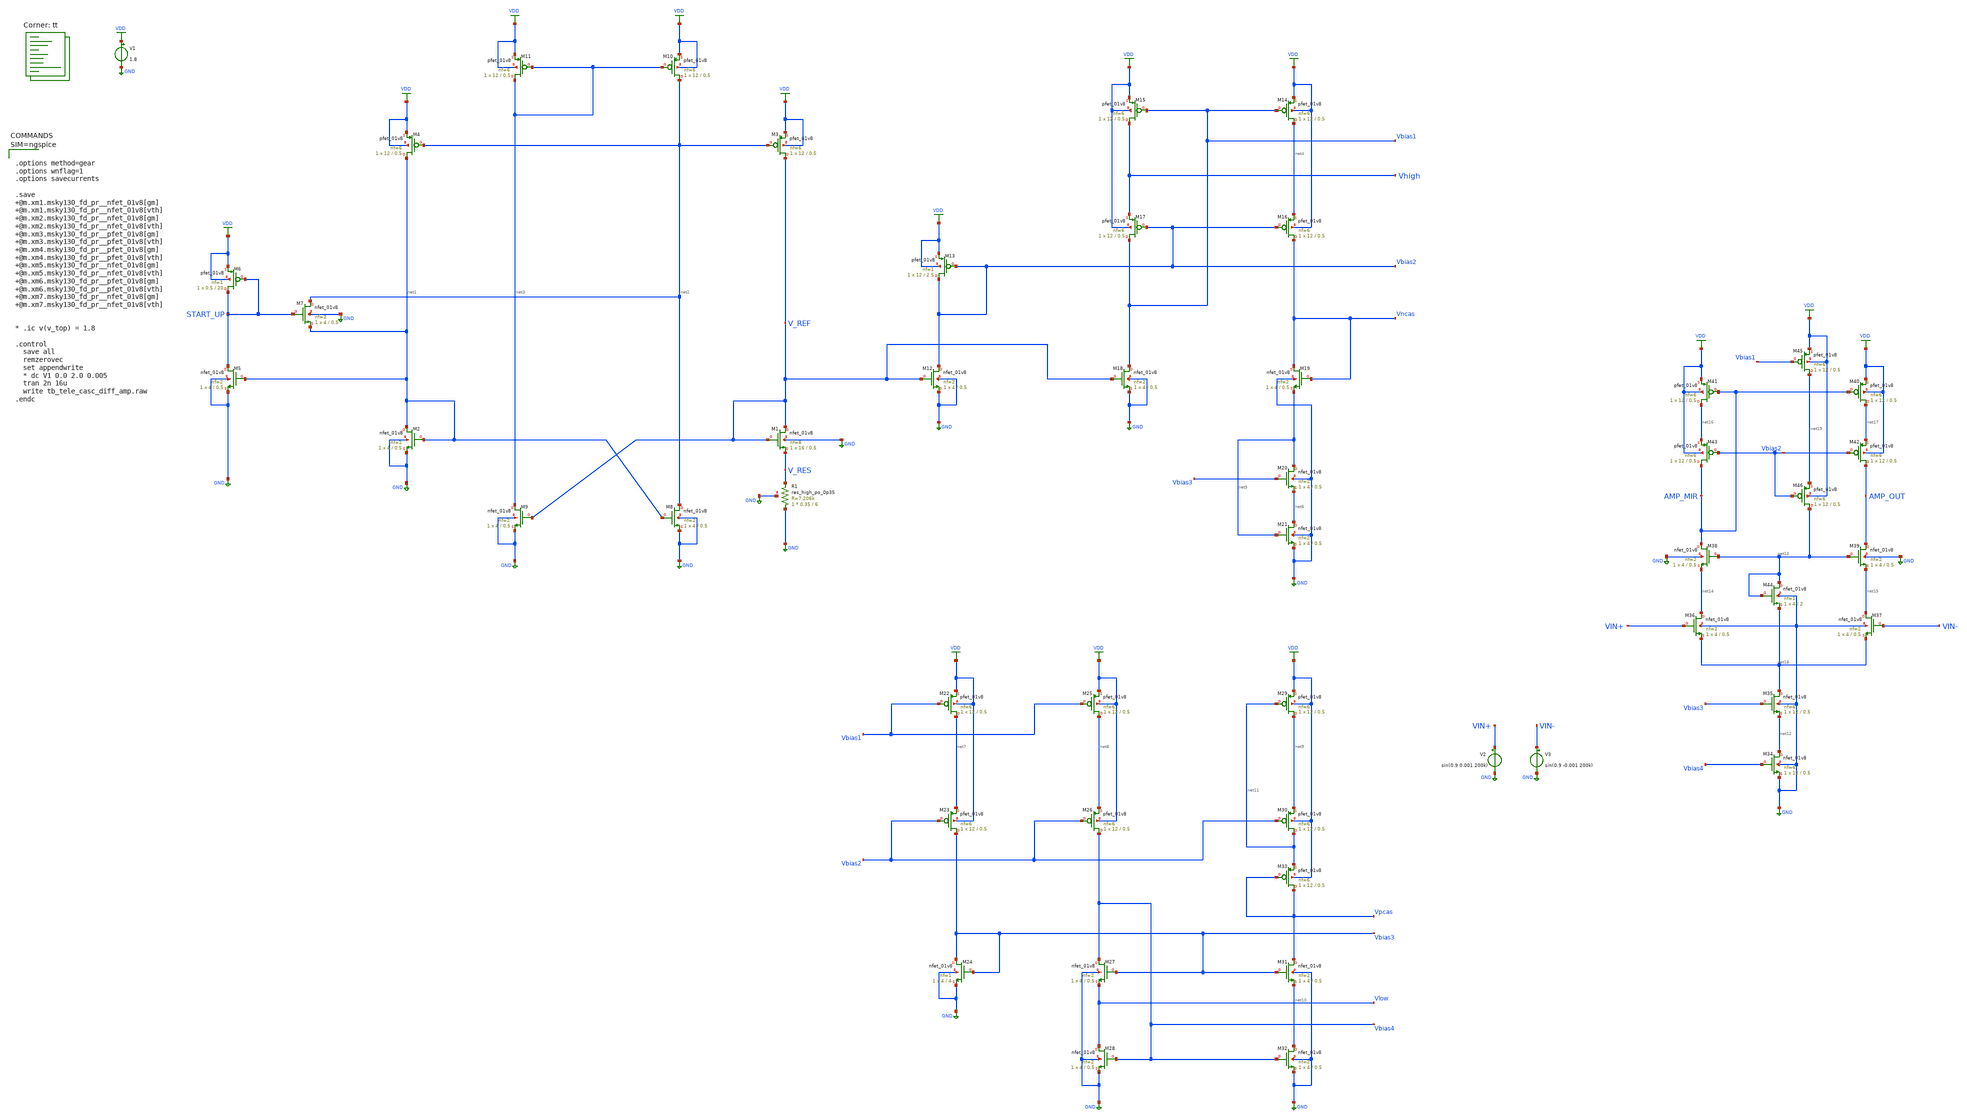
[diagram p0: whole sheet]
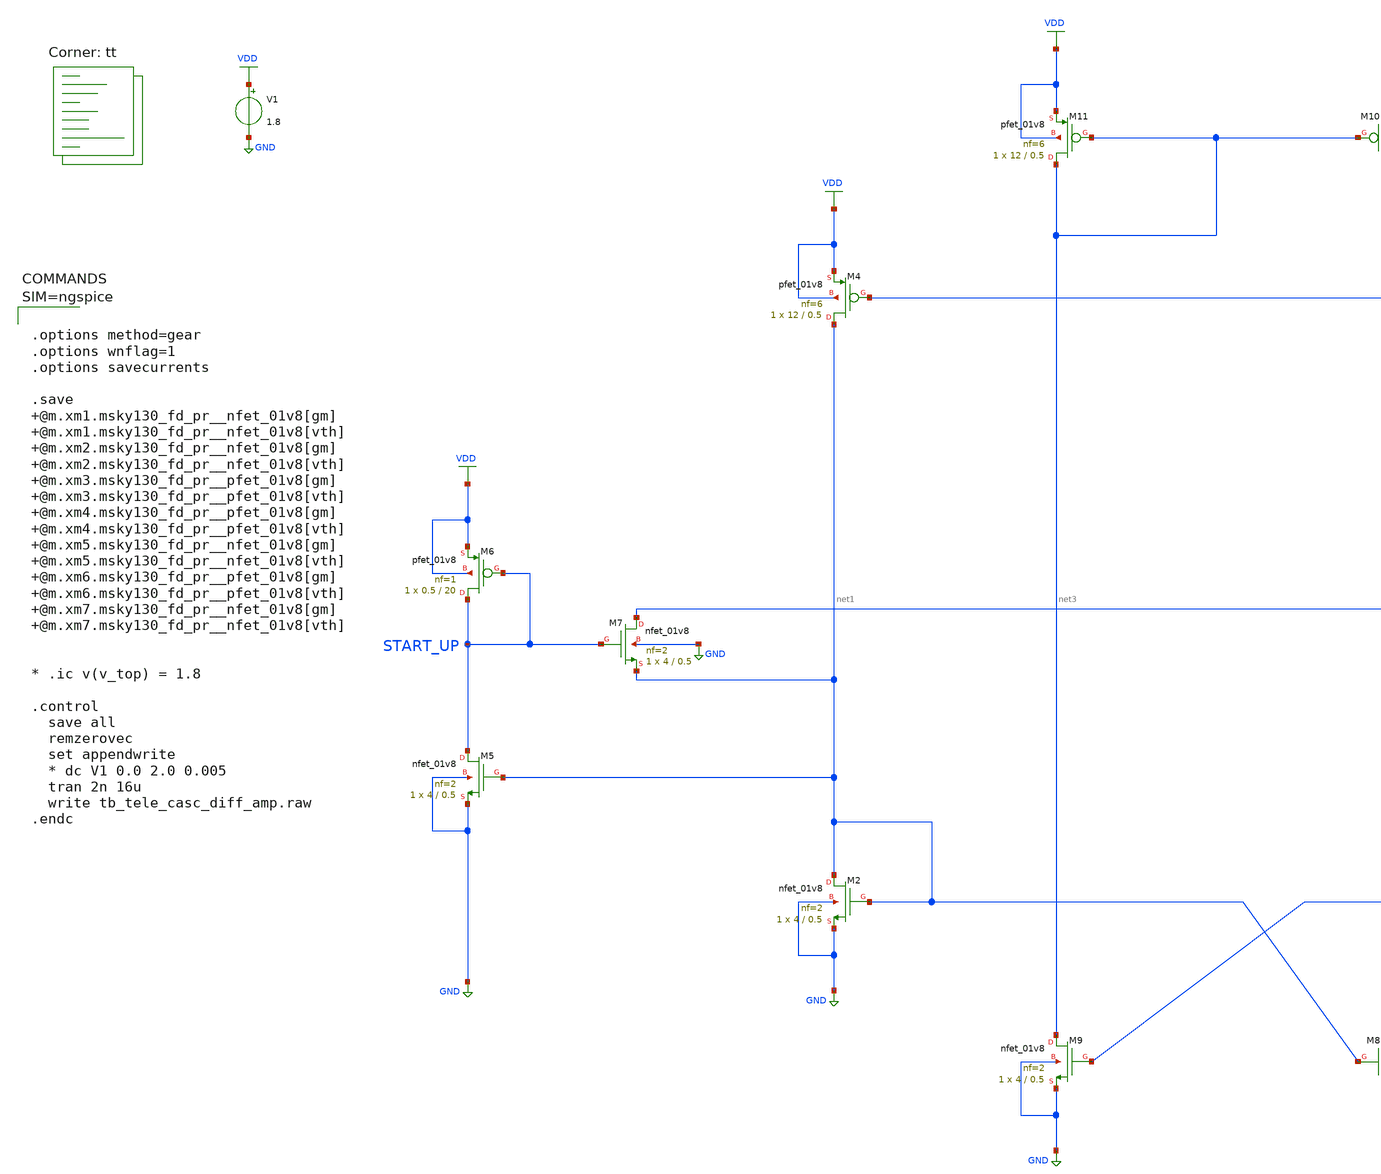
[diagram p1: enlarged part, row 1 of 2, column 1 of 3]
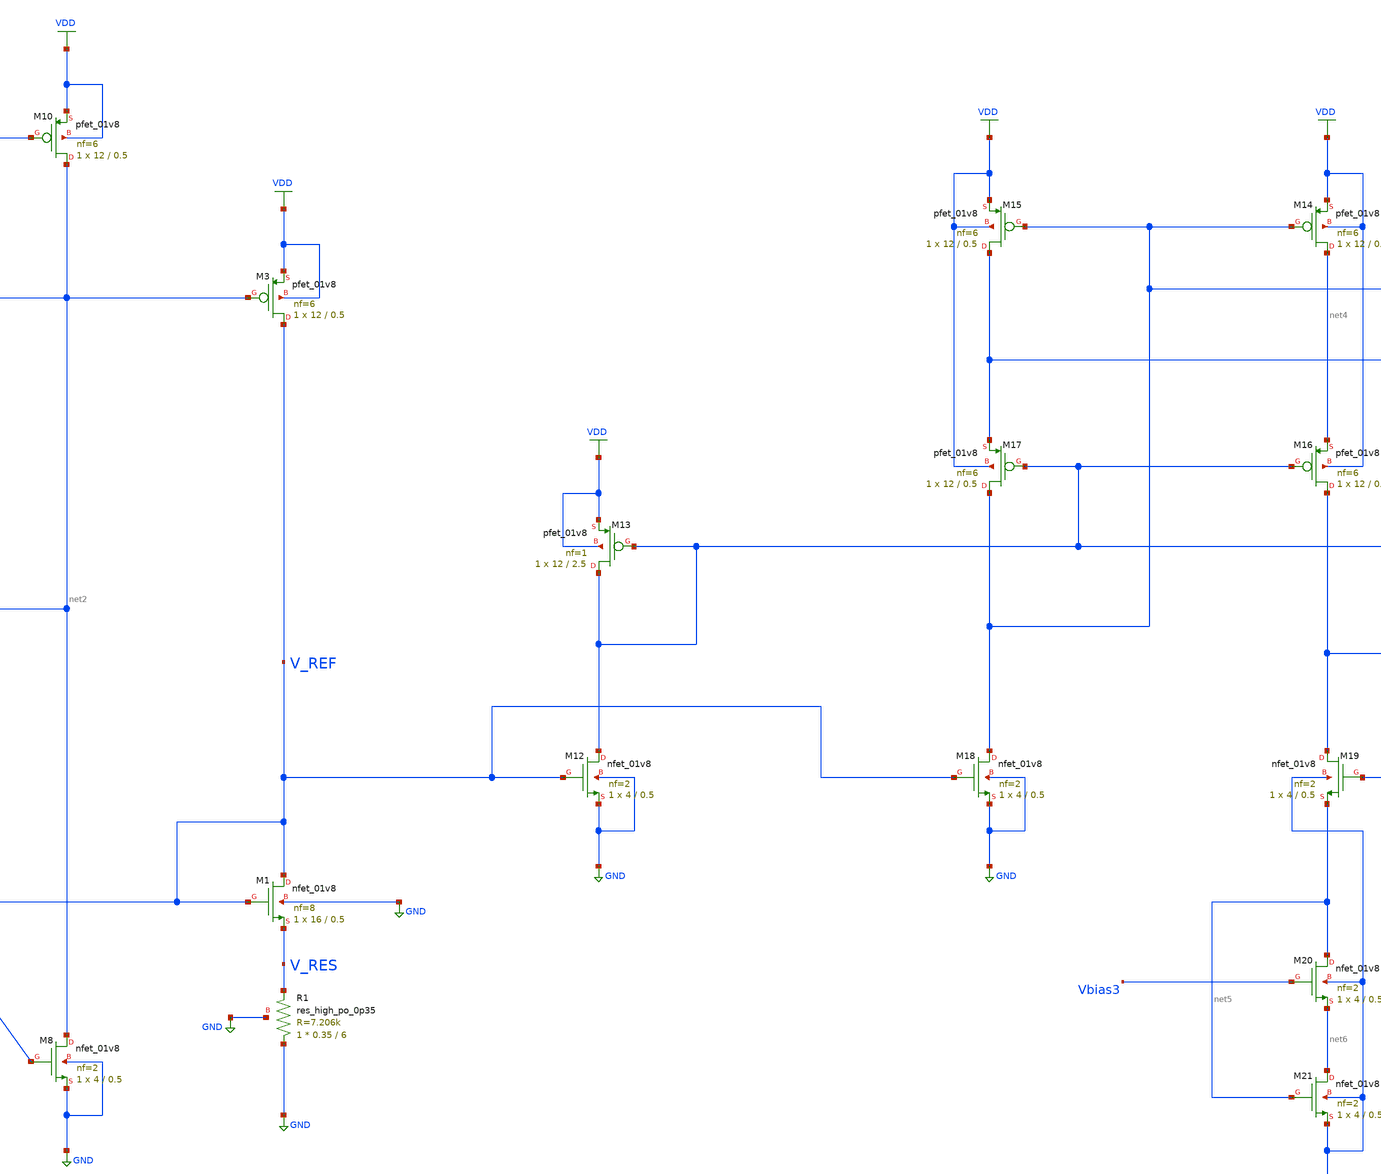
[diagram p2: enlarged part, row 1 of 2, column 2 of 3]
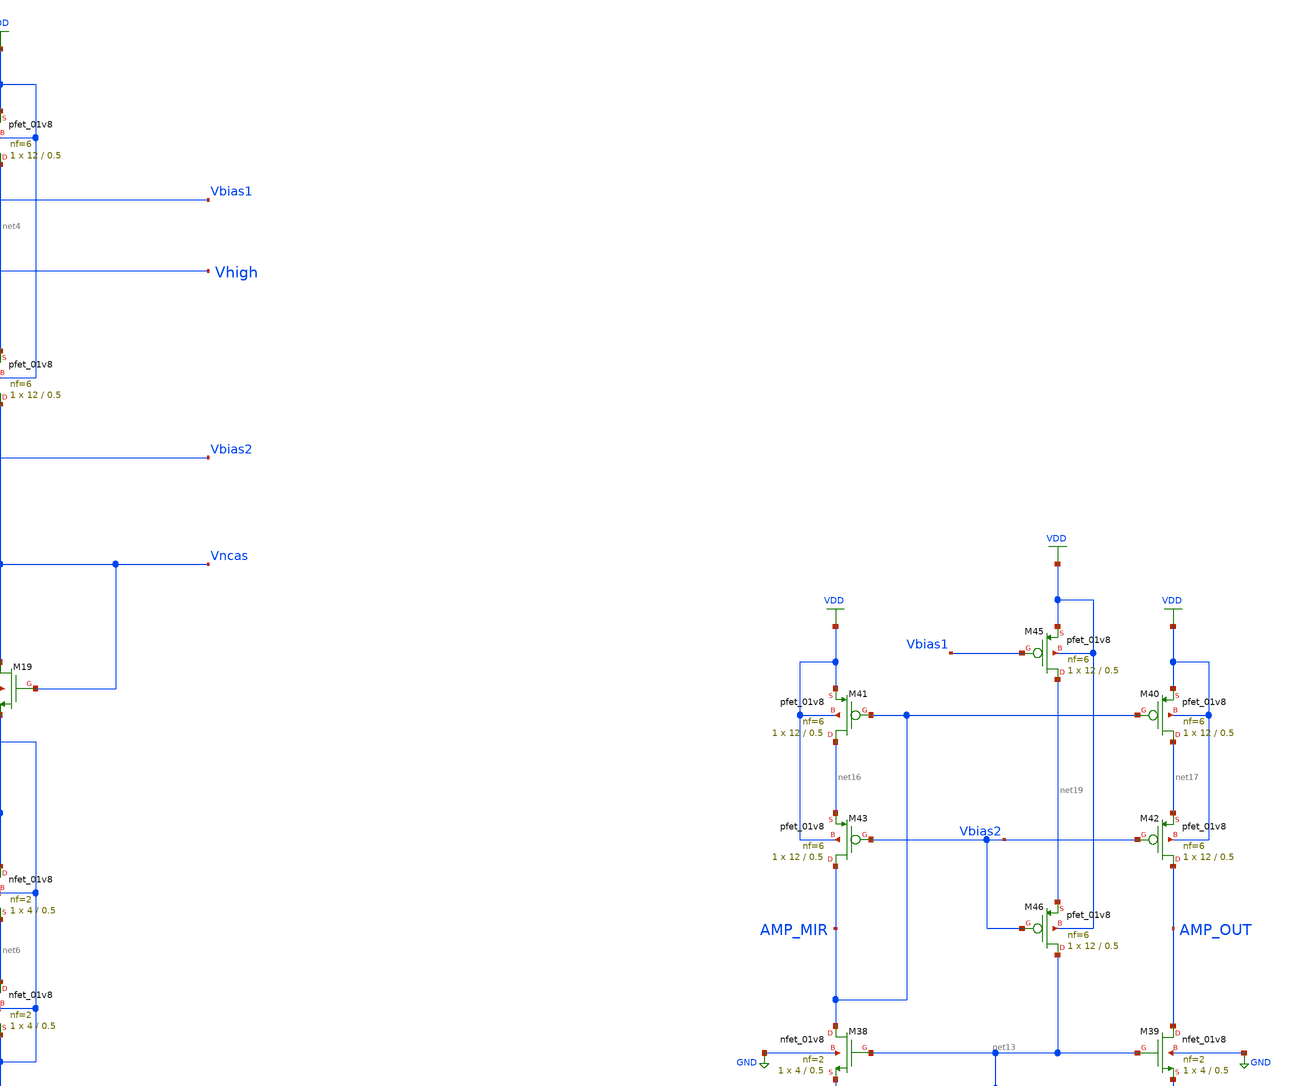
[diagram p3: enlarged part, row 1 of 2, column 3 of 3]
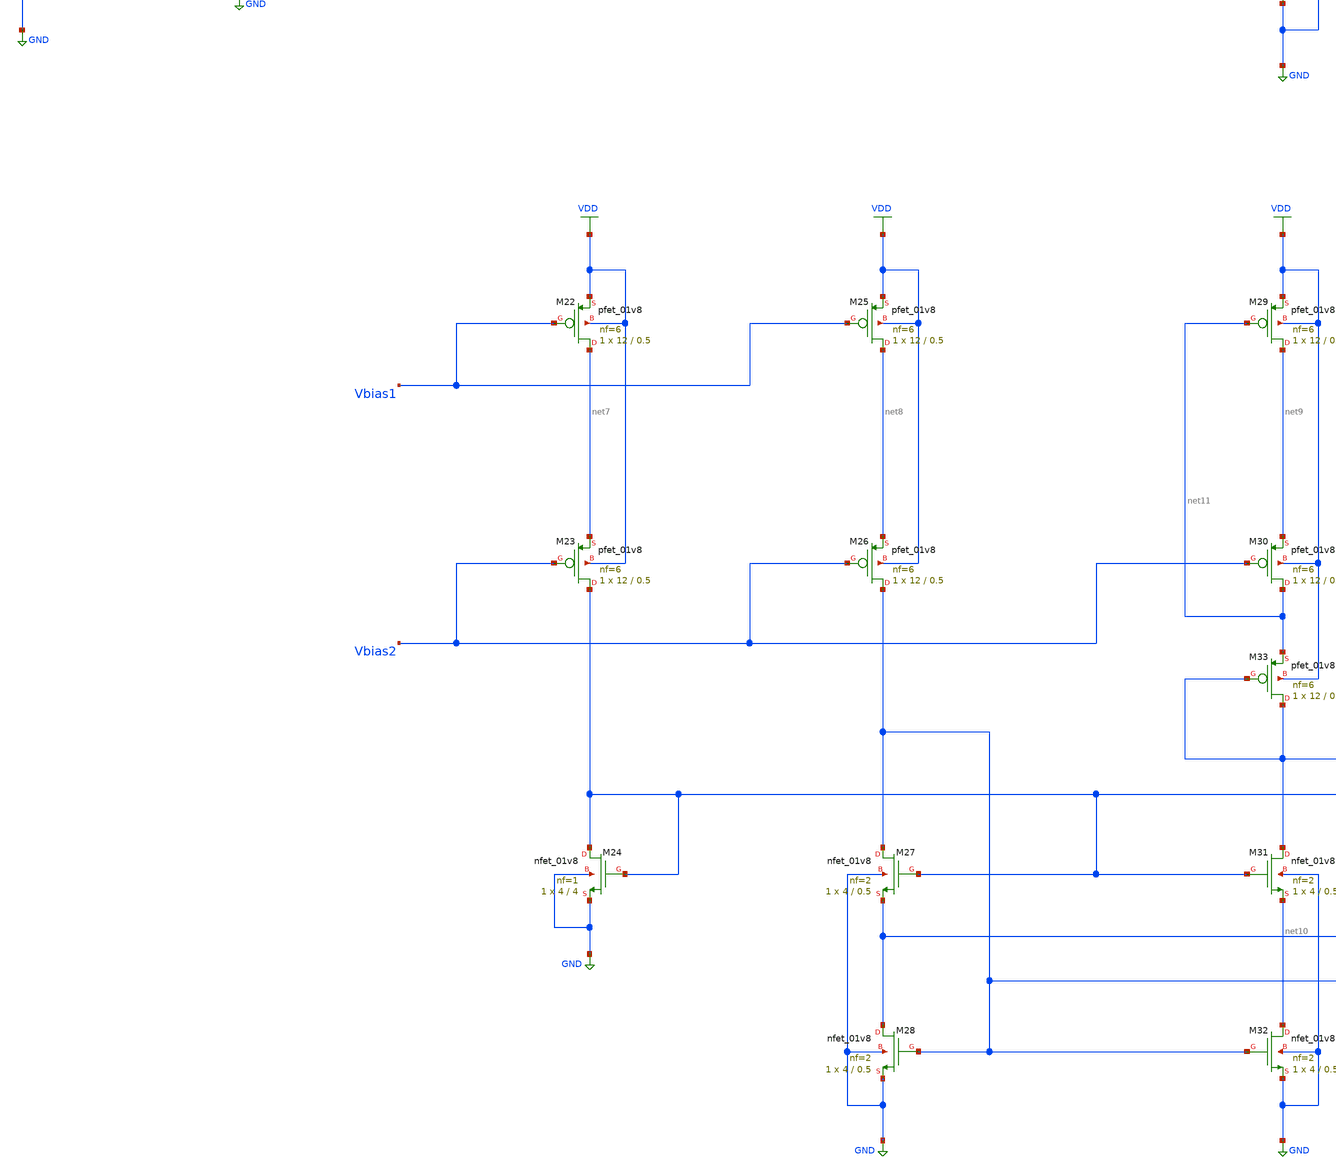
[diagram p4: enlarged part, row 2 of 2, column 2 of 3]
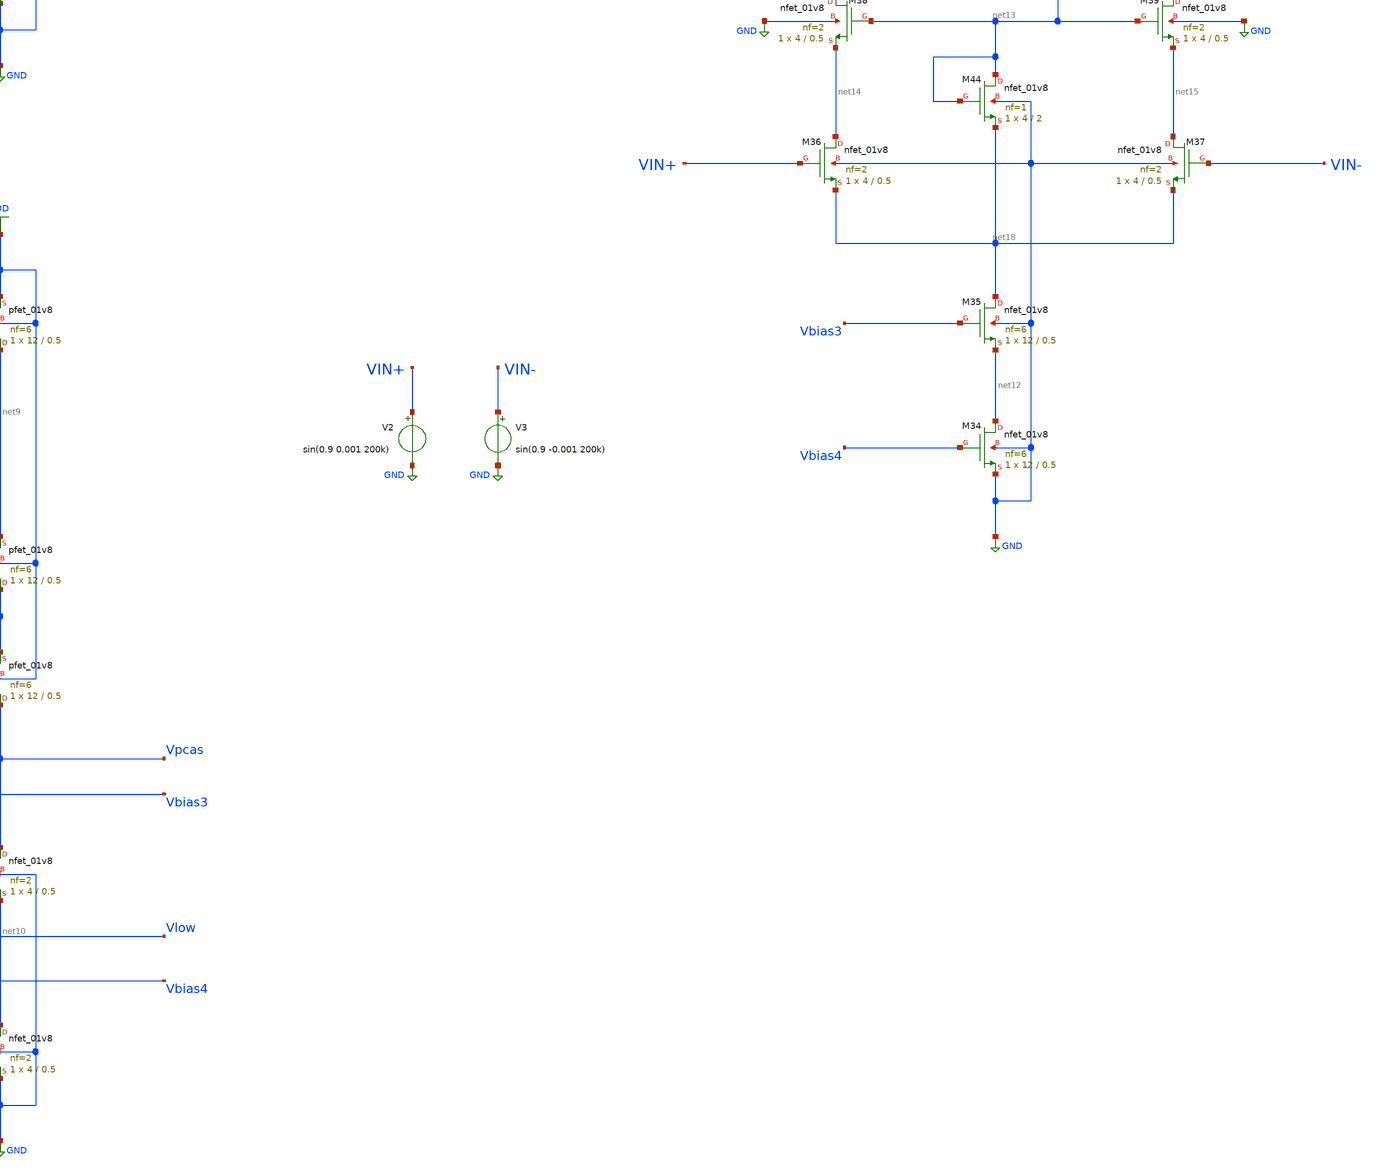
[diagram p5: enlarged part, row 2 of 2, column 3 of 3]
** sch_path: projects/ASU/EEE572/schematic/tb_tele_casc_diff_amp.sch
**.subckt tb_tele_casc_diff_amp
V1 VDD GND 1.8
XM1 V_REF V_REF V_RES GND sky130_fd_pr__nfet_01v8 L=0.5 W=16 nf=8 ad='int((nf+1)/2) * W/nf * 0.29' as='int((nf+2)/2) * W/nf * 0.29'
+ pd='2*int((nf+1)/2) * (W/nf + 0.29)' ps='2*int((nf+2)/2) * (W/nf + 0.29)' nrd='0.29 / W' nrs='0.29 / W'
+ sa=0 sb=0 sd=0 mult=1 m=1
XM2 net1 net1 GND GND sky130_fd_pr__nfet_01v8 L=0.5 W=4 nf=2 ad='int((nf+1)/2) * W/nf * 0.29' as='int((nf+2)/2) * W/nf * 0.29'
+ pd='2*int((nf+1)/2) * (W/nf + 0.29)' ps='2*int((nf+2)/2) * (W/nf + 0.29)' nrd='0.29 / W' nrs='0.29 / W'
+ sa=0 sb=0 sd=0 mult=1 m=1
XM5 START_UP net1 GND GND sky130_fd_pr__nfet_01v8 L=0.5 W=4 nf=2 ad='int((nf+1)/2) * W/nf * 0.29' as='int((nf+2)/2) * W/nf * 0.29'
+ pd='2*int((nf+1)/2) * (W/nf + 0.29)' ps='2*int((nf+2)/2) * (W/nf + 0.29)' nrd='0.29 / W' nrs='0.29 / W'
+ sa=0 sb=0 sd=0 mult=1 m=1
XM7 net2 START_UP net1 GND sky130_fd_pr__nfet_01v8 L=0.5 W=4 nf=2 ad='int((nf+1)/2) * W/nf * 0.29' as='int((nf+2)/2) * W/nf * 0.29'
+ pd='2*int((nf+1)/2) * (W/nf + 0.29)' ps='2*int((nf+2)/2) * (W/nf + 0.29)' nrd='0.29 / W' nrs='0.29 / W'
+ sa=0 sb=0 sd=0 mult=1 m=1
XR1 GND V_RES GND sky130_fd_pr__res_high_po_0p35 L=6 mult=1 m=1
XM6 START_UP START_UP VDD VDD sky130_fd_pr__pfet_01v8 L=20 W=0.5 nf=1 ad='int((nf+1)/2) * W/nf * 0.29'
+ as='int((nf+2)/2) * W/nf * 0.29' pd='2*int((nf+1)/2) * (W/nf + 0.29)' ps='2*int((nf+2)/2) * (W/nf + 0.29)'
+ nrd='0.29 / W' nrs='0.29 / W' sa=0 sb=0 sd=0 mult=1 m=1
XM3 V_REF net2 VDD VDD sky130_fd_pr__pfet_01v8 L=0.5 W=12 nf=6 ad='int((nf+1)/2) * W/nf * 0.29' as='int((nf+2)/2) * W/nf * 0.29'
+ pd='2*int((nf+1)/2) * (W/nf + 0.29)' ps='2*int((nf+2)/2) * (W/nf + 0.29)' nrd='0.29 / W' nrs='0.29 / W'
+ sa=0 sb=0 sd=0 mult=1 m=1
XM4 net1 net2 VDD VDD sky130_fd_pr__pfet_01v8 L=0.5 W=12 nf=6 ad='int((nf+1)/2) * W/nf * 0.29' as='int((nf+2)/2) * W/nf * 0.29'
+ pd='2*int((nf+1)/2) * (W/nf + 0.29)' ps='2*int((nf+2)/2) * (W/nf + 0.29)' nrd='0.29 / W' nrs='0.29 / W'
+ sa=0 sb=0 sd=0 mult=1 m=1
XM8 net2 net1 GND GND sky130_fd_pr__nfet_01v8 L=0.5 W=4 nf=2 ad='int((nf+1)/2) * W/nf * 0.29' as='int((nf+2)/2) * W/nf * 0.29'
+ pd='2*int((nf+1)/2) * (W/nf + 0.29)' ps='2*int((nf+2)/2) * (W/nf + 0.29)' nrd='0.29 / W' nrs='0.29 / W'
+ sa=0 sb=0 sd=0 mult=1 m=1
XM9 net3 V_REF GND GND sky130_fd_pr__nfet_01v8 L=0.5 W=4 nf=2 ad='int((nf+1)/2) * W/nf * 0.29' as='int((nf+2)/2) * W/nf * 0.29'
+ pd='2*int((nf+1)/2) * (W/nf + 0.29)' ps='2*int((nf+2)/2) * (W/nf + 0.29)' nrd='0.29 / W' nrs='0.29 / W'
+ sa=0 sb=0 sd=0 mult=1 m=1
XM10 net2 net3 VDD VDD sky130_fd_pr__pfet_01v8 L=0.5 W=12 nf=6 ad='int((nf+1)/2) * W/nf * 0.29' as='int((nf+2)/2) * W/nf * 0.29'
+ pd='2*int((nf+1)/2) * (W/nf + 0.29)' ps='2*int((nf+2)/2) * (W/nf + 0.29)' nrd='0.29 / W' nrs='0.29 / W'
+ sa=0 sb=0 sd=0 mult=1 m=1
XM11 net3 net3 VDD VDD sky130_fd_pr__pfet_01v8 L=0.5 W=12 nf=6 ad='int((nf+1)/2) * W/nf * 0.29' as='int((nf+2)/2) * W/nf * 0.29'
+ pd='2*int((nf+1)/2) * (W/nf + 0.29)' ps='2*int((nf+2)/2) * (W/nf + 0.29)' nrd='0.29 / W' nrs='0.29 / W'
+ sa=0 sb=0 sd=0 mult=1 m=1
XM12 Vbias2 V_REF GND GND sky130_fd_pr__nfet_01v8 L=0.5 W=4 nf=2 ad='int((nf+1)/2) * W/nf * 0.29' as='int((nf+2)/2) * W/nf * 0.29'
+ pd='2*int((nf+1)/2) * (W/nf + 0.29)' ps='2*int((nf+2)/2) * (W/nf + 0.29)' nrd='0.29 / W' nrs='0.29 / W'
+ sa=0 sb=0 sd=0 mult=1 m=1
XM13 Vbias2 Vbias2 VDD VDD sky130_fd_pr__pfet_01v8 L=2.5 W=12 nf=1 ad='int((nf+1)/2) * W/nf * 0.29' as='int((nf+2)/2) * W/nf * 0.29'
+ pd='2*int((nf+1)/2) * (W/nf + 0.29)' ps='2*int((nf+2)/2) * (W/nf + 0.29)' nrd='0.29 / W' nrs='0.29 / W'
+ sa=0 sb=0 sd=0 mult=1 m=1
XM14 net4 Vbias1 VDD VDD sky130_fd_pr__pfet_01v8 L=0.5 W=12 nf=6 ad='int((nf+1)/2) * W/nf * 0.29' as='int((nf+2)/2) * W/nf * 0.29'
+ pd='2*int((nf+1)/2) * (W/nf + 0.29)' ps='2*int((nf+2)/2) * (W/nf + 0.29)' nrd='0.29 / W' nrs='0.29 / W'
+ sa=0 sb=0 sd=0 mult=1 m=1
XM15 Vhigh Vbias1 VDD VDD sky130_fd_pr__pfet_01v8 L=0.5 W=12 nf=6 ad='int((nf+1)/2) * W/nf * 0.29' as='int((nf+2)/2) * W/nf * 0.29'
+ pd='2*int((nf+1)/2) * (W/nf + 0.29)' ps='2*int((nf+2)/2) * (W/nf + 0.29)' nrd='0.29 / W' nrs='0.29 / W'
+ sa=0 sb=0 sd=0 mult=1 m=1
XM16 Vncas Vbias2 net4 VDD sky130_fd_pr__pfet_01v8 L=0.5 W=12 nf=6 ad='int((nf+1)/2) * W/nf * 0.29' as='int((nf+2)/2) * W/nf * 0.29'
+ pd='2*int((nf+1)/2) * (W/nf + 0.29)' ps='2*int((nf+2)/2) * (W/nf + 0.29)' nrd='0.29 / W' nrs='0.29 / W'
+ sa=0 sb=0 sd=0 mult=1 m=1
XM17 Vbias1 Vbias2 Vhigh VDD sky130_fd_pr__pfet_01v8 L=0.5 W=12 nf=6 ad='int((nf+1)/2) * W/nf * 0.29'
+ as='int((nf+2)/2) * W/nf * 0.29' pd='2*int((nf+1)/2) * (W/nf + 0.29)' ps='2*int((nf+2)/2) * (W/nf + 0.29)'
+ nrd='0.29 / W' nrs='0.29 / W' sa=0 sb=0 sd=0 mult=1 m=1
XM18 Vbias1 V_REF GND GND sky130_fd_pr__nfet_01v8 L=0.5 W=4 nf=2 ad='int((nf+1)/2) * W/nf * 0.29' as='int((nf+2)/2) * W/nf * 0.29'
+ pd='2*int((nf+1)/2) * (W/nf + 0.29)' ps='2*int((nf+2)/2) * (W/nf + 0.29)' nrd='0.29 / W' nrs='0.29 / W'
+ sa=0 sb=0 sd=0 mult=1 m=1
XM19 Vncas Vncas net5 GND sky130_fd_pr__nfet_01v8 L=0.5 W=4 nf=2 ad='int((nf+1)/2) * W/nf * 0.29' as='int((nf+2)/2) * W/nf * 0.29'
+ pd='2*int((nf+1)/2) * (W/nf + 0.29)' ps='2*int((nf+2)/2) * (W/nf + 0.29)' nrd='0.29 / W' nrs='0.29 / W'
+ sa=0 sb=0 sd=0 mult=1 m=1
XM20 net5 Vbias3 net6 GND sky130_fd_pr__nfet_01v8 L=0.5 W=4 nf=2 ad='int((nf+1)/2) * W/nf * 0.29' as='int((nf+2)/2) * W/nf * 0.29'
+ pd='2*int((nf+1)/2) * (W/nf + 0.29)' ps='2*int((nf+2)/2) * (W/nf + 0.29)' nrd='0.29 / W' nrs='0.29 / W'
+ sa=0 sb=0 sd=0 mult=1 m=1
XM21 net6 net5 GND GND sky130_fd_pr__nfet_01v8 L=0.5 W=4 nf=2 ad='int((nf+1)/2) * W/nf * 0.29' as='int((nf+2)/2) * W/nf * 0.29'
+ pd='2*int((nf+1)/2) * (W/nf + 0.29)' ps='2*int((nf+2)/2) * (W/nf + 0.29)' nrd='0.29 / W' nrs='0.29 / W'
+ sa=0 sb=0 sd=0 mult=1 m=1
XM22 net7 Vbias1 VDD VDD sky130_fd_pr__pfet_01v8 L=0.5 W=12 nf=6 ad='int((nf+1)/2) * W/nf * 0.29' as='int((nf+2)/2) * W/nf * 0.29'
+ pd='2*int((nf+1)/2) * (W/nf + 0.29)' ps='2*int((nf+2)/2) * (W/nf + 0.29)' nrd='0.29 / W' nrs='0.29 / W'
+ sa=0 sb=0 sd=0 mult=1 m=1
XM23 Vbias3 Vbias2 net7 VDD sky130_fd_pr__pfet_01v8 L=0.5 W=12 nf=6 ad='int((nf+1)/2) * W/nf * 0.29'
+ as='int((nf+2)/2) * W/nf * 0.29' pd='2*int((nf+1)/2) * (W/nf + 0.29)' ps='2*int((nf+2)/2) * (W/nf + 0.29)'
+ nrd='0.29 / W' nrs='0.29 / W' sa=0 sb=0 sd=0 mult=1 m=1
XM24 Vbias3 Vbias3 GND GND sky130_fd_pr__nfet_01v8 L=4 W=4 nf=1 ad='int((nf+1)/2) * W/nf * 0.29' as='int((nf+2)/2) * W/nf * 0.29'
+ pd='2*int((nf+1)/2) * (W/nf + 0.29)' ps='2*int((nf+2)/2) * (W/nf + 0.29)' nrd='0.29 / W' nrs='0.29 / W'
+ sa=0 sb=0 sd=0 mult=1 m=1
XM25 net8 Vbias1 VDD VDD sky130_fd_pr__pfet_01v8 L=0.5 W=12 nf=6 ad='int((nf+1)/2) * W/nf * 0.29' as='int((nf+2)/2) * W/nf * 0.29'
+ pd='2*int((nf+1)/2) * (W/nf + 0.29)' ps='2*int((nf+2)/2) * (W/nf + 0.29)' nrd='0.29 / W' nrs='0.29 / W'
+ sa=0 sb=0 sd=0 mult=1 m=1
XM26 Vbias4 Vbias2 net8 VDD sky130_fd_pr__pfet_01v8 L=0.5 W=12 nf=6 ad='int((nf+1)/2) * W/nf * 0.29'
+ as='int((nf+2)/2) * W/nf * 0.29' pd='2*int((nf+1)/2) * (W/nf + 0.29)' ps='2*int((nf+2)/2) * (W/nf + 0.29)'
+ nrd='0.29 / W' nrs='0.29 / W' sa=0 sb=0 sd=0 mult=1 m=1
XM27 Vbias4 Vbias3 Vlow GND sky130_fd_pr__nfet_01v8 L=0.5 W=4 nf=2 ad='int((nf+1)/2) * W/nf * 0.29' as='int((nf+2)/2) * W/nf * 0.29'
+ pd='2*int((nf+1)/2) * (W/nf + 0.29)' ps='2*int((nf+2)/2) * (W/nf + 0.29)' nrd='0.29 / W' nrs='0.29 / W'
+ sa=0 sb=0 sd=0 mult=1 m=1
XM28 Vlow Vbias4 GND GND sky130_fd_pr__nfet_01v8 L=0.5 W=4 nf=2 ad='int((nf+1)/2) * W/nf * 0.29' as='int((nf+2)/2) * W/nf * 0.29'
+ pd='2*int((nf+1)/2) * (W/nf + 0.29)' ps='2*int((nf+2)/2) * (W/nf + 0.29)' nrd='0.29 / W' nrs='0.29 / W'
+ sa=0 sb=0 sd=0 mult=1 m=1
XM29 net9 net11 VDD VDD sky130_fd_pr__pfet_01v8 L=0.5 W=12 nf=6 ad='int((nf+1)/2) * W/nf * 0.29' as='int((nf+2)/2) * W/nf * 0.29'
+ pd='2*int((nf+1)/2) * (W/nf + 0.29)' ps='2*int((nf+2)/2) * (W/nf + 0.29)' nrd='0.29 / W' nrs='0.29 / W'
+ sa=0 sb=0 sd=0 mult=1 m=1
XM30 net11 Vbias2 net9 VDD sky130_fd_pr__pfet_01v8 L=0.5 W=12 nf=6 ad='int((nf+1)/2) * W/nf * 0.29' as='int((nf+2)/2) * W/nf * 0.29'
+ pd='2*int((nf+1)/2) * (W/nf + 0.29)' ps='2*int((nf+2)/2) * (W/nf + 0.29)' nrd='0.29 / W' nrs='0.29 / W'
+ sa=0 sb=0 sd=0 mult=1 m=1
XM31 Vpcas Vbias3 net10 GND sky130_fd_pr__nfet_01v8 L=0.5 W=4 nf=2 ad='int((nf+1)/2) * W/nf * 0.29' as='int((nf+2)/2) * W/nf * 0.29'
+ pd='2*int((nf+1)/2) * (W/nf + 0.29)' ps='2*int((nf+2)/2) * (W/nf + 0.29)' nrd='0.29 / W' nrs='0.29 / W'
+ sa=0 sb=0 sd=0 mult=1 m=1
XM32 net10 Vbias4 GND GND sky130_fd_pr__nfet_01v8 L=0.5 W=4 nf=2 ad='int((nf+1)/2) * W/nf * 0.29' as='int((nf+2)/2) * W/nf * 0.29'
+ pd='2*int((nf+1)/2) * (W/nf + 0.29)' ps='2*int((nf+2)/2) * (W/nf + 0.29)' nrd='0.29 / W' nrs='0.29 / W'
+ sa=0 sb=0 sd=0 mult=1 m=1
XM33 Vpcas Vpcas net11 VDD sky130_fd_pr__pfet_01v8 L=0.5 W=12 nf=6 ad='int((nf+1)/2) * W/nf * 0.29' as='int((nf+2)/2) * W/nf * 0.29'
+ pd='2*int((nf+1)/2) * (W/nf + 0.29)' ps='2*int((nf+2)/2) * (W/nf + 0.29)' nrd='0.29 / W' nrs='0.29 / W'
+ sa=0 sb=0 sd=0 mult=1 m=1
XM34 net12 Vbias4 GND GND sky130_fd_pr__nfet_01v8 L=0.5 W=12 nf=6 ad='int((nf+1)/2) * W/nf * 0.29' as='int((nf+2)/2) * W/nf * 0.29'
+ pd='2*int((nf+1)/2) * (W/nf + 0.29)' ps='2*int((nf+2)/2) * (W/nf + 0.29)' nrd='0.29 / W' nrs='0.29 / W'
+ sa=0 sb=0 sd=0 mult=1 m=1
XM35 net18 Vbias3 net12 GND sky130_fd_pr__nfet_01v8 L=0.5 W=12 nf=6 ad='int((nf+1)/2) * W/nf * 0.29'
+ as='int((nf+2)/2) * W/nf * 0.29' pd='2*int((nf+1)/2) * (W/nf + 0.29)' ps='2*int((nf+2)/2) * (W/nf + 0.29)'
+ nrd='0.29 / W' nrs='0.29 / W' sa=0 sb=0 sd=0 mult=1 m=1
XM36 net14 VIN+ net18 GND sky130_fd_pr__nfet_01v8 L=0.5 W=4 nf=2 ad='int((nf+1)/2) * W/nf * 0.29' as='int((nf+2)/2) * W/nf * 0.29'
+ pd='2*int((nf+1)/2) * (W/nf + 0.29)' ps='2*int((nf+2)/2) * (W/nf + 0.29)' nrd='0.29 / W' nrs='0.29 / W'
+ sa=0 sb=0 sd=0 mult=1 m=1
XM37 net15 VIN- net18 GND sky130_fd_pr__nfet_01v8 L=0.5 W=4 nf=2 ad='int((nf+1)/2) * W/nf * 0.29' as='int((nf+2)/2) * W/nf * 0.29'
+ pd='2*int((nf+1)/2) * (W/nf + 0.29)' ps='2*int((nf+2)/2) * (W/nf + 0.29)' nrd='0.29 / W' nrs='0.29 / W'
+ sa=0 sb=0 sd=0 mult=1 m=1
XM38 AMP_MIR net13 net14 GND sky130_fd_pr__nfet_01v8 L=0.5 W=4 nf=2 ad='int((nf+1)/2) * W/nf * 0.29'
+ as='int((nf+2)/2) * W/nf * 0.29' pd='2*int((nf+1)/2) * (W/nf + 0.29)' ps='2*int((nf+2)/2) * (W/nf + 0.29)'
+ nrd='0.29 / W' nrs='0.29 / W' sa=0 sb=0 sd=0 mult=1 m=1
XM39 AMP_OUT net13 net15 GND sky130_fd_pr__nfet_01v8 L=0.5 W=4 nf=2 ad='int((nf+1)/2) * W/nf * 0.29'
+ as='int((nf+2)/2) * W/nf * 0.29' pd='2*int((nf+1)/2) * (W/nf + 0.29)' ps='2*int((nf+2)/2) * (W/nf + 0.29)'
+ nrd='0.29 / W' nrs='0.29 / W' sa=0 sb=0 sd=0 mult=1 m=1
XM40 net17 AMP_MIR VDD VDD sky130_fd_pr__pfet_01v8 L=0.5 W=12 nf=6 ad='int((nf+1)/2) * W/nf * 0.29' as='int((nf+2)/2) * W/nf * 0.29'
+ pd='2*int((nf+1)/2) * (W/nf + 0.29)' ps='2*int((nf+2)/2) * (W/nf + 0.29)' nrd='0.29 / W' nrs='0.29 / W'
+ sa=0 sb=0 sd=0 mult=1 m=1
XM41 net16 AMP_MIR VDD VDD sky130_fd_pr__pfet_01v8 L=0.5 W=12 nf=6 ad='int((nf+1)/2) * W/nf * 0.29' as='int((nf+2)/2) * W/nf * 0.29'
+ pd='2*int((nf+1)/2) * (W/nf + 0.29)' ps='2*int((nf+2)/2) * (W/nf + 0.29)' nrd='0.29 / W' nrs='0.29 / W'
+ sa=0 sb=0 sd=0 mult=1 m=1
XM42 AMP_OUT Vbias2 net17 VDD sky130_fd_pr__pfet_01v8 L=0.5 W=12 nf=6 ad='int((nf+1)/2) * W/nf * 0.29'
+ as='int((nf+2)/2) * W/nf * 0.29' pd='2*int((nf+1)/2) * (W/nf + 0.29)' ps='2*int((nf+2)/2) * (W/nf + 0.29)'
+ nrd='0.29 / W' nrs='0.29 / W' sa=0 sb=0 sd=0 mult=1 m=1
XM43 AMP_MIR Vbias2 net16 VDD sky130_fd_pr__pfet_01v8 L=0.5 W=12 nf=6 ad='int((nf+1)/2) * W/nf * 0.29'
+ as='int((nf+2)/2) * W/nf * 0.29' pd='2*int((nf+1)/2) * (W/nf + 0.29)' ps='2*int((nf+2)/2) * (W/nf + 0.29)'
+ nrd='0.29 / W' nrs='0.29 / W' sa=0 sb=0 sd=0 mult=1 m=1
XM44 net13 net13 net18 GND sky130_fd_pr__nfet_01v8 L=2 W=4 nf=1 ad='int((nf+1)/2) * W/nf * 0.29' as='int((nf+2)/2) * W/nf * 0.29'
+ pd='2*int((nf+1)/2) * (W/nf + 0.29)' ps='2*int((nf+2)/2) * (W/nf + 0.29)' nrd='0.29 / W' nrs='0.29 / W'
+ sa=0 sb=0 sd=0 mult=1 m=1
XM45 net19 Vbias1 VDD VDD sky130_fd_pr__pfet_01v8 L=0.5 W=12 nf=6 ad='int((nf+1)/2) * W/nf * 0.29' as='int((nf+2)/2) * W/nf * 0.29'
+ pd='2*int((nf+1)/2) * (W/nf + 0.29)' ps='2*int((nf+2)/2) * (W/nf + 0.29)' nrd='0.29 / W' nrs='0.29 / W'
+ sa=0 sb=0 sd=0 mult=1 m=1
XM46 net13 Vbias2 net19 VDD sky130_fd_pr__pfet_01v8 L=0.5 W=12 nf=6 ad='int((nf+1)/2) * W/nf * 0.29'
+ as='int((nf+2)/2) * W/nf * 0.29' pd='2*int((nf+1)/2) * (W/nf + 0.29)' ps='2*int((nf+2)/2) * (W/nf + 0.29)'
+ nrd='0.29 / W' nrs='0.29 / W' sa=0 sb=0 sd=0 mult=1 m=1
V3 VIN- GND sin(0.9 -0.001 200k)
V2 VIN+ GND sin(0.9 0.001 200k)
**** begin user architecture code
.lib $::SKYWATER_MODELS/sky130.lib.spice tt



.options method=gear
.options wnflag=1
.options savecurrents

.save @m.xm1.msky130_fd_pr__nfet_01v8[gm] @m.xm1.msky130_fd_pr__nfet_01v8[vth] @m.xm2.msky130_fd_pr__nfet_01v8[gm] @m.xm2.msky130_fd_pr__nfet_01v8[vth] @m.xm3.msky130_fd_pr__pfet_01v8[gm] @m.xm3.msky130_fd_pr__pfet_01v8[vth] @m.xm4.msky130_fd_pr__pfet_01v8[gm] @m.xm4.msky130_fd_pr__pfet_01v8[vth] @m.xm5.msky130_fd_pr__nfet_01v8[gm] @m.xm5.msky130_fd_pr__nfet_01v8[vth] @m.xm6.msky130_fd_pr__pfet_01v8[gm] @m.xm6.msky130_fd_pr__pfet_01v8[vth] @m.xm7.msky130_fd_pr__nfet_01v8[gm] @m.xm7.msky130_fd_pr__nfet_01v8[vth]


* .ic v(v_top) = 1.8

.control
  save all
  remzerovec
  set appendwrite
  * dc V1 0.0 2.0 0.005
  tran 2n 16u
  write tb_tele_casc_diff_amp.raw
.endc





**** end user architecture code
**.ends
.GLOBAL GND
.GLOBAL VDD
.end
